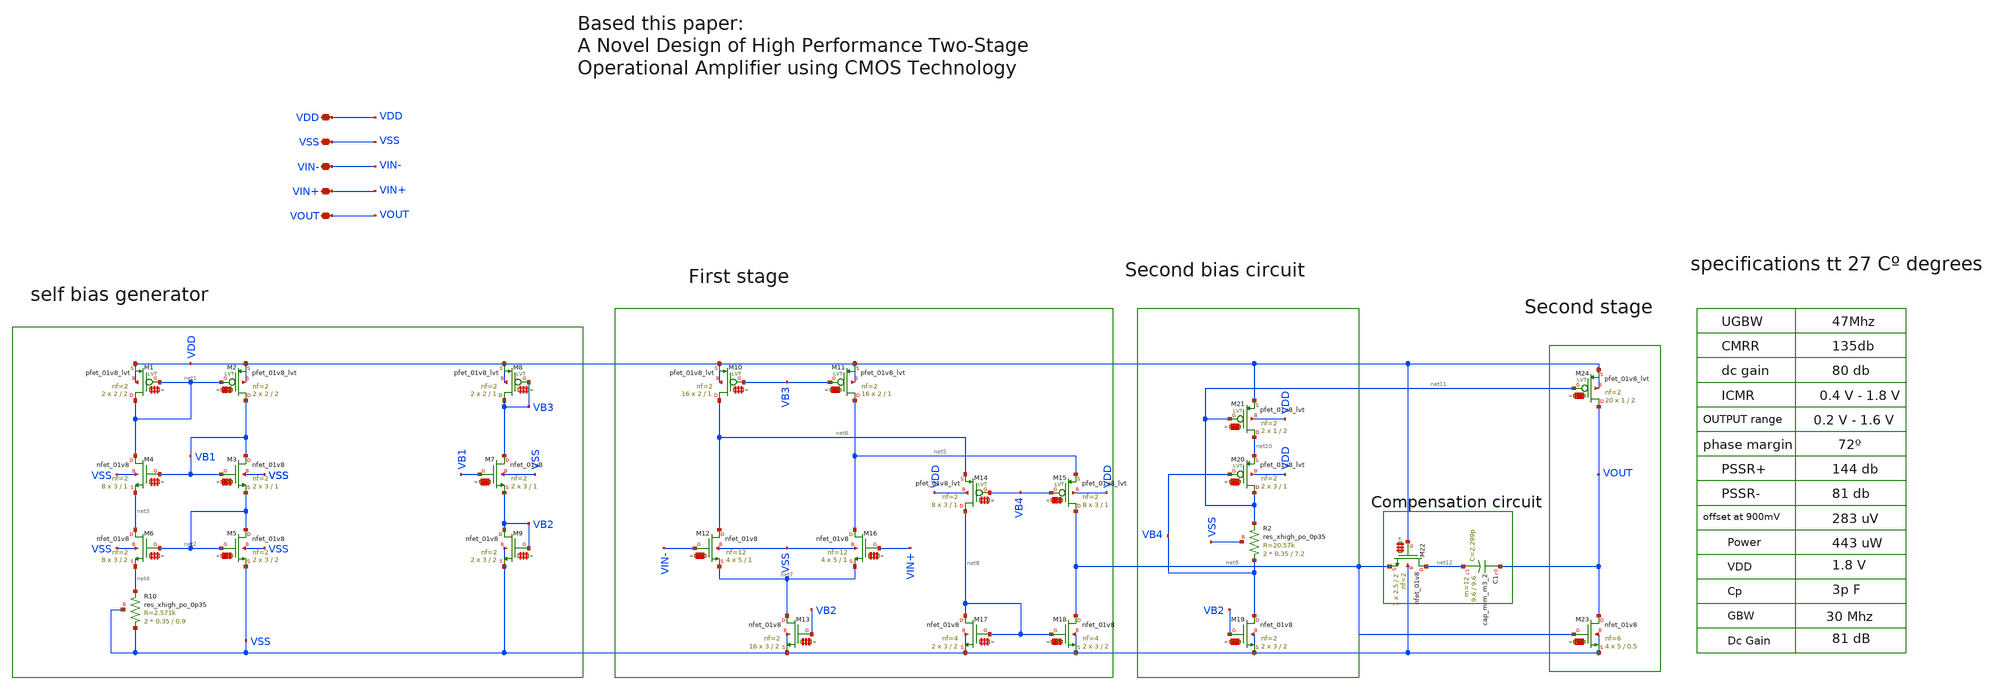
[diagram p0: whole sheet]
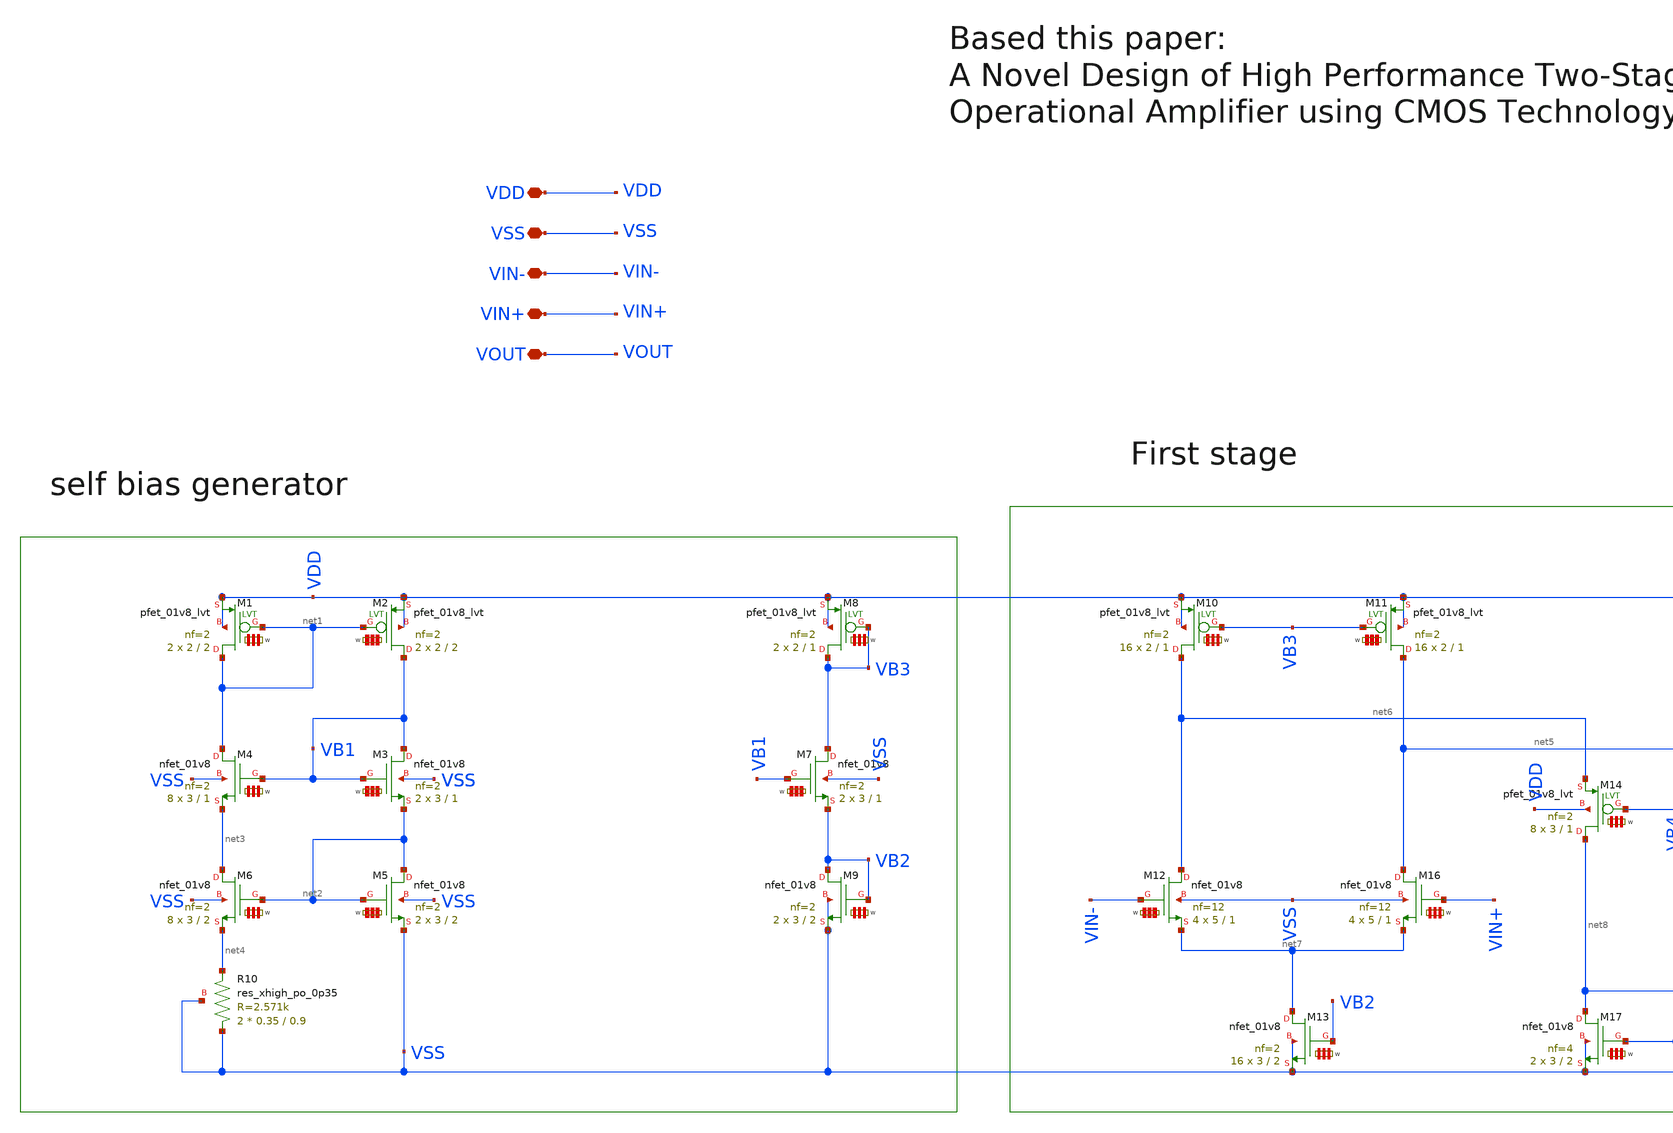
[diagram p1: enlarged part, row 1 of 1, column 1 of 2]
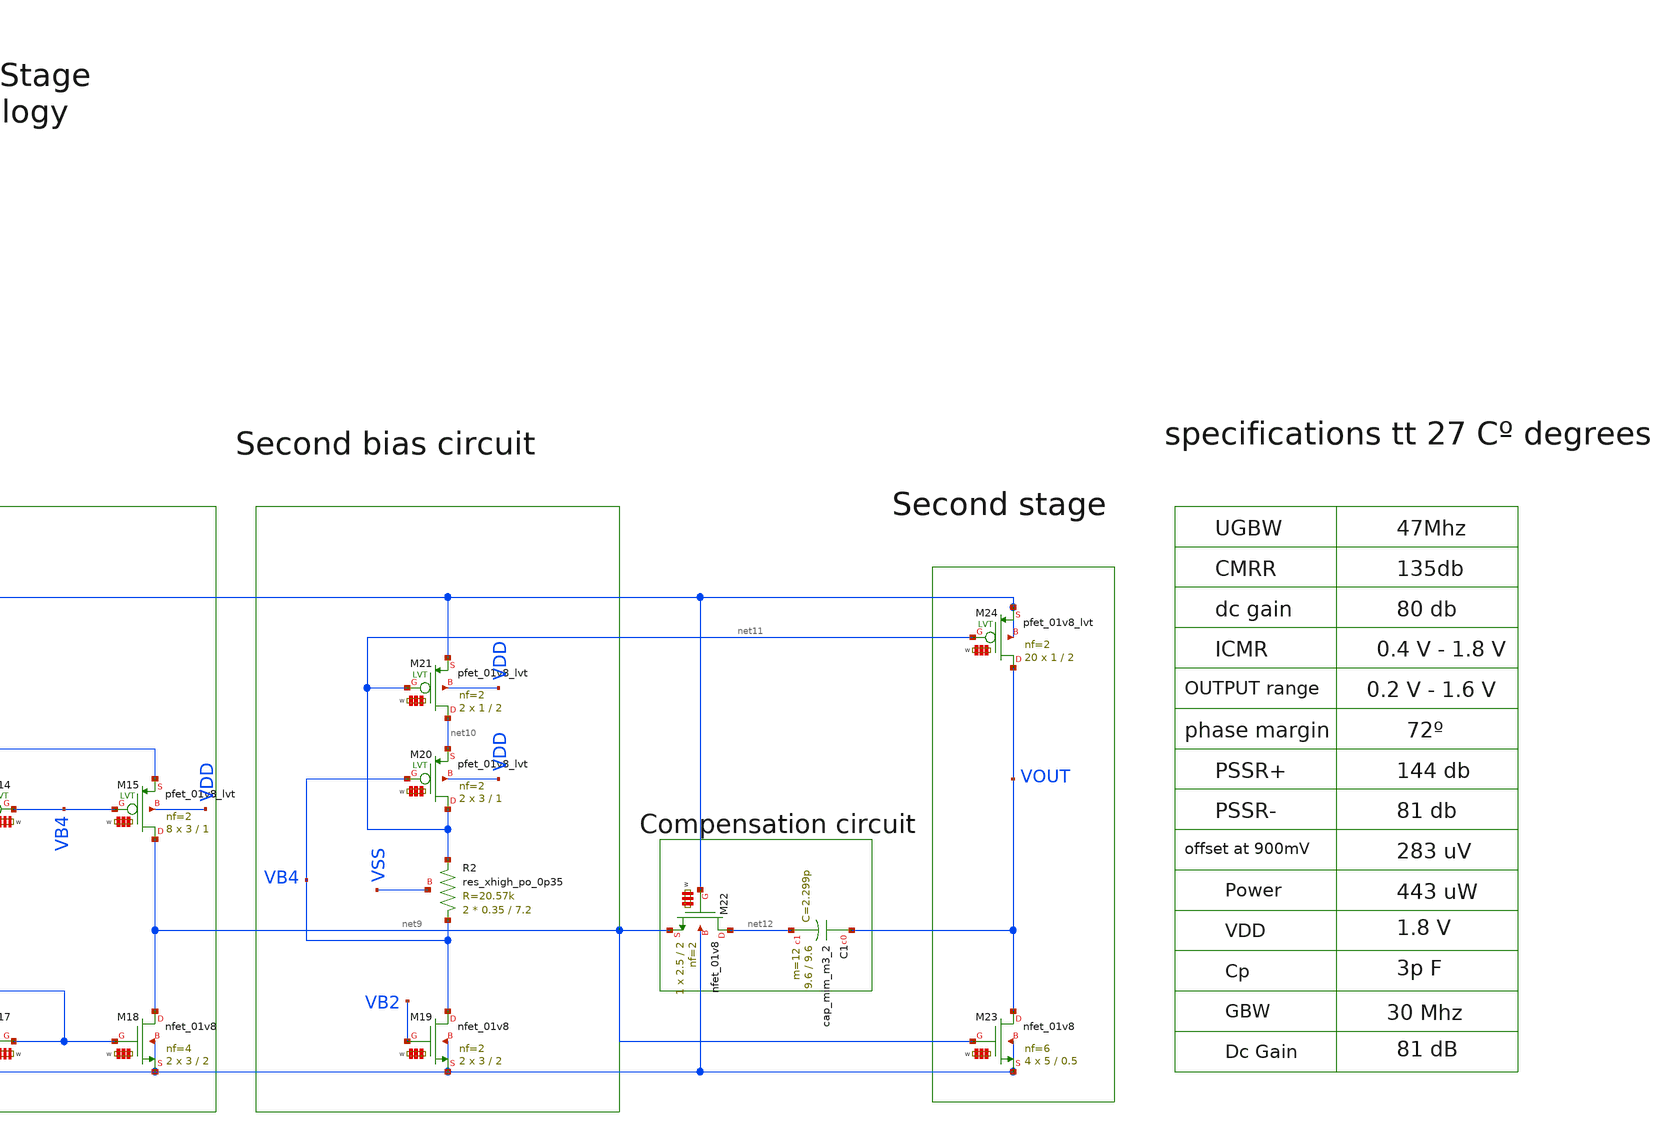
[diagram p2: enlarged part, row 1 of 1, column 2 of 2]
** sch_path: LIB/Sky130A/single ended amplifiers/VA002_NMOS_1.8_sky130A.sch
**.subckt VA002_NMOS_1.8_sky130A VDD VSS VIN- VIN+ VOUT
*.iopin VDD
*.iopin VSS
*.iopin VIN-
*.iopin VIN+
*.iopin VOUT
XR10 VSS net4 VSS sky130_fd_pr__res_xhigh_po_0p35 L=0.9 mult=2 m=2
XM4 net1 VB1 net3 VSS sky130_fd_pr__nfet_01v8 L=1 W='3 * 2 ' nf=2 ad='int((2 + 1)/2) * 3 / 2 * 0.29'
+ as='int((2 + 2)/2) * 3 / 2 * 0.29' pd='2*int((2 + 1)/2) * (3 / 2 + 0.29)' ps='2*int((2 + 2)/2) * (3 / 2 + 0.29)'
+ nrd='0.29 / 3 ' nrs='0.29 / 3 ' sa=0 sb=0 sd=0 mult=8 m=8
XM3 VB1 VB1 net2 VSS sky130_fd_pr__nfet_01v8 L=1 W='3 * 2 ' nf=2 ad='int((2 + 1)/2) * 3 / 2 * 0.29' as='int((2 + 2)/2) * 3 / 2 * 0.29'
+ pd='2*int((2 + 1)/2) * (3 / 2 + 0.29)' ps='2*int((2 + 2)/2) * (3 / 2 + 0.29)' nrd='0.29 / 3 ' nrs='0.29 / 3 '
+ sa=0 sb=0 sd=0 mult=2 m=2
XM6 net3 net2 net4 VSS sky130_fd_pr__nfet_01v8 L=2 W='3 * 2 ' nf=2 ad='int((2 + 1)/2) * 3 / 2 * 0.29'
+ as='int((2 + 2)/2) * 3 / 2 * 0.29' pd='2*int((2 + 1)/2) * (3 / 2 + 0.29)' ps='2*int((2 + 2)/2) * (3 / 2 + 0.29)'
+ nrd='0.29 / 3 ' nrs='0.29 / 3 ' sa=0 sb=0 sd=0 mult=8 m=8
XM5 net2 net2 VSS VSS sky130_fd_pr__nfet_01v8 L=2 W='3 * 2 ' nf=2 ad='int((2 + 1)/2) * 3 / 2 * 0.29'
+ as='int((2 + 2)/2) * 3 / 2 * 0.29' pd='2*int((2 + 1)/2) * (3 / 2 + 0.29)' ps='2*int((2 + 2)/2) * (3 / 2 + 0.29)'
+ nrd='0.29 / 3 ' nrs='0.29 / 3 ' sa=0 sb=0 sd=0 mult=2 m=2
XM7 VB3 VB1 VB2 VSS sky130_fd_pr__nfet_01v8 L=1 W='3 * 2 ' nf=2 ad='int((2 + 1)/2) * 3 / 2 * 0.29' as='int((2 + 2)/2) * 3 / 2 * 0.29'
+ pd='2*int((2 + 1)/2) * (3 / 2 + 0.29)' ps='2*int((2 + 2)/2) * (3 / 2 + 0.29)' nrd='0.29 / 3 ' nrs='0.29 / 3 '
+ sa=0 sb=0 sd=0 mult=2 m=2
XM9 VB2 VB2 VSS VSS sky130_fd_pr__nfet_01v8 L=2 W='3 * 2 ' nf=2 ad='int((2 + 1)/2) * 3 / 2 * 0.29' as='int((2 + 2)/2) * 3 / 2 * 0.29'
+ pd='2*int((2 + 1)/2) * (3 / 2 + 0.29)' ps='2*int((2 + 2)/2) * (3 / 2 + 0.29)' nrd='0.29 / 3 ' nrs='0.29 / 3 '
+ sa=0 sb=0 sd=0 mult=2 m=2
XM8 VB3 VB3 VDD VDD sky130_fd_pr__pfet_01v8_lvt L=1 W='2 * 2 ' nf=2 ad='int((2 + 1)/2) * 2 / 2 * 0.29'
+ as='int((2 + 2)/2) * 2 / 2 * 0.29' pd='2*int((2 + 1)/2) * (2 / 2 + 0.29)' ps='2*int((2 + 2)/2) * (2 / 2 + 0.29)'
+ nrd='0.29 / 2 ' nrs='0.29 / 2 ' sa=0 sb=0 sd=0 mult=2 m=2
XM1 net1 net1 VDD VDD sky130_fd_pr__pfet_01v8_lvt L=2 W='2 * 2 ' nf=2 ad='int((2 + 1)/2) * 2 / 2 * 0.29'
+ as='int((2 + 2)/2) * 2 / 2 * 0.29' pd='2*int((2 + 1)/2) * (2 / 2 + 0.29)' ps='2*int((2 + 2)/2) * (2 / 2 + 0.29)'
+ nrd='0.29 / 2 ' nrs='0.29 / 2 ' sa=0 sb=0 sd=0 mult=2 m=2
XM2 VB1 net1 VDD VDD sky130_fd_pr__pfet_01v8_lvt L=2 W='2 * 2 ' nf=2 ad='int((2 + 1)/2) * 2 / 2 * 0.29'
+ as='int((2 + 2)/2) * 2 / 2 * 0.29' pd='2*int((2 + 1)/2) * (2 / 2 + 0.29)' ps='2*int((2 + 2)/2) * (2 / 2 + 0.29)'
+ nrd='0.29 / 2 ' nrs='0.29 / 2 ' sa=0 sb=0 sd=0 mult=2 m=2
XM10 net6 VB3 VDD VDD sky130_fd_pr__pfet_01v8_lvt L=1 W='2 * 2 ' nf=2 ad='int((2 + 1)/2) * 2 / 2 * 0.29'
+ as='int((2 + 2)/2) * 2 / 2 * 0.29' pd='2*int((2 + 1)/2) * (2 / 2 + 0.29)' ps='2*int((2 + 2)/2) * (2 / 2 + 0.29)'
+ nrd='0.29 / 2 ' nrs='0.29 / 2 ' sa=0 sb=0 sd=0 mult=16 m=16
XM11 net5 VB3 VDD VDD sky130_fd_pr__pfet_01v8_lvt L=1 W='2 * 2 ' nf=2 ad='int((2 + 1)/2) * 2 / 2 * 0.29'
+ as='int((2 + 2)/2) * 2 / 2 * 0.29' pd='2*int((2 + 1)/2) * (2 / 2 + 0.29)' ps='2*int((2 + 2)/2) * (2 / 2 + 0.29)'
+ nrd='0.29 / 2 ' nrs='0.29 / 2 ' sa=0 sb=0 sd=0 mult=16 m=16
XM12 net6 VIN- net7 VSS sky130_fd_pr__nfet_01v8 L=1 W='5 * 12 ' nf=12 ad='int((12 + 1)/2) * 5 / 12 * 0.29'
+ as='int((12 + 2)/2) * 5 / 12 * 0.29' pd='2*int((12 + 1)/2) * (5 / 12 + 0.29)' ps='2*int((12 + 2)/2) * (5 / 12 + 0.29)'
+ nrd='0.29 / 5 ' nrs='0.29 / 5 ' sa=0 sb=0 sd=0 mult=4 m=4
XM13 net7 VB2 VSS VSS sky130_fd_pr__nfet_01v8 L=2 W='3 * 2 ' nf=2 ad='int((2 + 1)/2) * 3 / 2 * 0.29'
+ as='int((2 + 2)/2) * 3 / 2 * 0.29' pd='2*int((2 + 1)/2) * (3 / 2 + 0.29)' ps='2*int((2 + 2)/2) * (3 / 2 + 0.29)'
+ nrd='0.29 / 3 ' nrs='0.29 / 3 ' sa=0 sb=0 sd=0 mult=16 m=16
XM14 net8 VB4 net6 VDD sky130_fd_pr__pfet_01v8_lvt L=1 W='3 * 2 ' nf=2 ad='int((2 + 1)/2) * 3 / 2 * 0.29'
+ as='int((2 + 2)/2) * 3 / 2 * 0.29' pd='2*int((2 + 1)/2) * (3 / 2 + 0.29)' ps='2*int((2 + 2)/2) * (3 / 2 + 0.29)'
+ nrd='0.29 / 3 ' nrs='0.29 / 3 ' sa=0 sb=0 sd=0 mult=8 m=8
XM15 net9 VB4 net5 VDD sky130_fd_pr__pfet_01v8_lvt L=1 W='3 * 2 ' nf=2 ad='int((2 + 1)/2) * 3 / 2 * 0.29'
+ as='int((2 + 2)/2) * 3 / 2 * 0.29' pd='2*int((2 + 1)/2) * (3 / 2 + 0.29)' ps='2*int((2 + 2)/2) * (3 / 2 + 0.29)'
+ nrd='0.29 / 3 ' nrs='0.29 / 3 ' sa=0 sb=0 sd=0 mult=8 m=8
XM16 net5 VIN+ net7 VSS sky130_fd_pr__nfet_01v8 L=1 W='5 * 12 ' nf=12 ad='int((12 + 1)/2) * 5 / 12 * 0.29'
+ as='int((12 + 2)/2) * 5 / 12 * 0.29' pd='2*int((12 + 1)/2) * (5 / 12 + 0.29)' ps='2*int((12 + 2)/2) * (5 / 12 + 0.29)'
+ nrd='0.29 / 5 ' nrs='0.29 / 5 ' sa=0 sb=0 sd=0 mult=4 m=4
XM17 net8 net8 VSS VSS sky130_fd_pr__nfet_01v8 L=2 W='3 * 4 ' nf=4 ad='int((4 + 1)/2) * 3 / 4 * 0.29'
+ as='int((4 + 2)/2) * 3 / 4 * 0.29' pd='2*int((4 + 1)/2) * (3 / 4 + 0.29)' ps='2*int((4 + 2)/2) * (3 / 4 + 0.29)'
+ nrd='0.29 / 3 ' nrs='0.29 / 3 ' sa=0 sb=0 sd=0 mult=2 m=2
XM18 net9 net8 VSS VSS sky130_fd_pr__nfet_01v8 L=2 W='3 * 4 ' nf=4 ad='int((4 + 1)/2) * 3 / 4 * 0.29'
+ as='int((4 + 2)/2) * 3 / 4 * 0.29' pd='2*int((4 + 1)/2) * (3 / 4 + 0.29)' ps='2*int((4 + 2)/2) * (3 / 4 + 0.29)'
+ nrd='0.29 / 3 ' nrs='0.29 / 3 ' sa=0 sb=0 sd=0 mult=2 m=2
XM19 VB4 VB2 VSS VSS sky130_fd_pr__nfet_01v8 L=2 W='3 * 2 ' nf=2 ad='int((2 + 1)/2) * 3 / 2 * 0.29' as='int((2 + 2)/2) * 3 / 2 * 0.29'
+ pd='2*int((2 + 1)/2) * (3 / 2 + 0.29)' ps='2*int((2 + 2)/2) * (3 / 2 + 0.29)' nrd='0.29 / 3 ' nrs='0.29 / 3 '
+ sa=0 sb=0 sd=0 mult=2 m=2
XR2 VB4 net11 VSS sky130_fd_pr__res_xhigh_po_0p35 L=7.2 mult=2 m=2
XM20 net11 VB4 net10 VDD sky130_fd_pr__pfet_01v8_lvt L=1 W='3 * 2 ' nf=2 ad='int((2 + 1)/2) * 3 / 2 * 0.29'
+ as='int((2 + 2)/2) * 3 / 2 * 0.29' pd='2*int((2 + 1)/2) * (3 / 2 + 0.29)' ps='2*int((2 + 2)/2) * (3 / 2 + 0.29)'
+ nrd='0.29 / 3 ' nrs='0.29 / 3 ' sa=0 sb=0 sd=0 mult=2 m=2
XM21 net10 net11 VDD VDD sky130_fd_pr__pfet_01v8_lvt L=2 W='1 * 2 ' nf=2 ad='int((2 + 1)/2) * 1 / 2 * 0.29'
+ as='int((2 + 2)/2) * 1 / 2 * 0.29' pd='2*int((2 + 1)/2) * (1 / 2 + 0.29)' ps='2*int((2 + 2)/2) * (1 / 2 + 0.29)'
+ nrd='0.29 / 1 ' nrs='0.29 / 1 ' sa=0 sb=0 sd=0 mult=2 m=2
XM22 net12 VDD net9 VSS sky130_fd_pr__nfet_01v8 L=2 W='2.5 * 2 ' nf=2 ad='int((2 + 1)/2) * 2.5 / 2 * 0.29'
+ as='int((2 + 2)/2) * 2.5 / 2 * 0.29' pd='2*int((2 + 1)/2) * (2.5 / 2 + 0.29)' ps='2*int((2 + 2)/2) * (2.5 / 2 + 0.29)'
+ nrd='0.29 / 2.5 ' nrs='0.29 / 2.5 ' sa=0 sb=0 sd=0 mult=1 m=1
XC1 VOUT net12 sky130_fd_pr__cap_mim_m3_2 W=9.6 L=9.6 MF=12 m=12
XM23 VOUT net9 VSS VSS sky130_fd_pr__nfet_01v8 L=0.5 W='5 * 6 ' nf=6 ad='int((6 + 1)/2) * 5 / 6 * 0.29'
+ as='int((6 + 2)/2) * 5 / 6 * 0.29' pd='2*int((6 + 1)/2) * (5 / 6 + 0.29)' ps='2*int((6 + 2)/2) * (5 / 6 + 0.29)'
+ nrd='0.29 / 5 ' nrs='0.29 / 5 ' sa=0 sb=0 sd=0 mult=4 m=4
XM24 VOUT net11 VDD VDD sky130_fd_pr__pfet_01v8_lvt L=2 W='1 * 2 ' nf=2 ad='int((2 + 1)/2) * 1 / 2 * 0.29'
+ as='int((2 + 2)/2) * 1 / 2 * 0.29' pd='2*int((2 + 1)/2) * (1 / 2 + 0.29)' ps='2*int((2 + 2)/2) * (1 / 2 + 0.29)'
+ nrd='0.29 / 1 ' nrs='0.29 / 1 ' sa=0 sb=0 sd=0 mult=20 m=20
**.ends
.end
